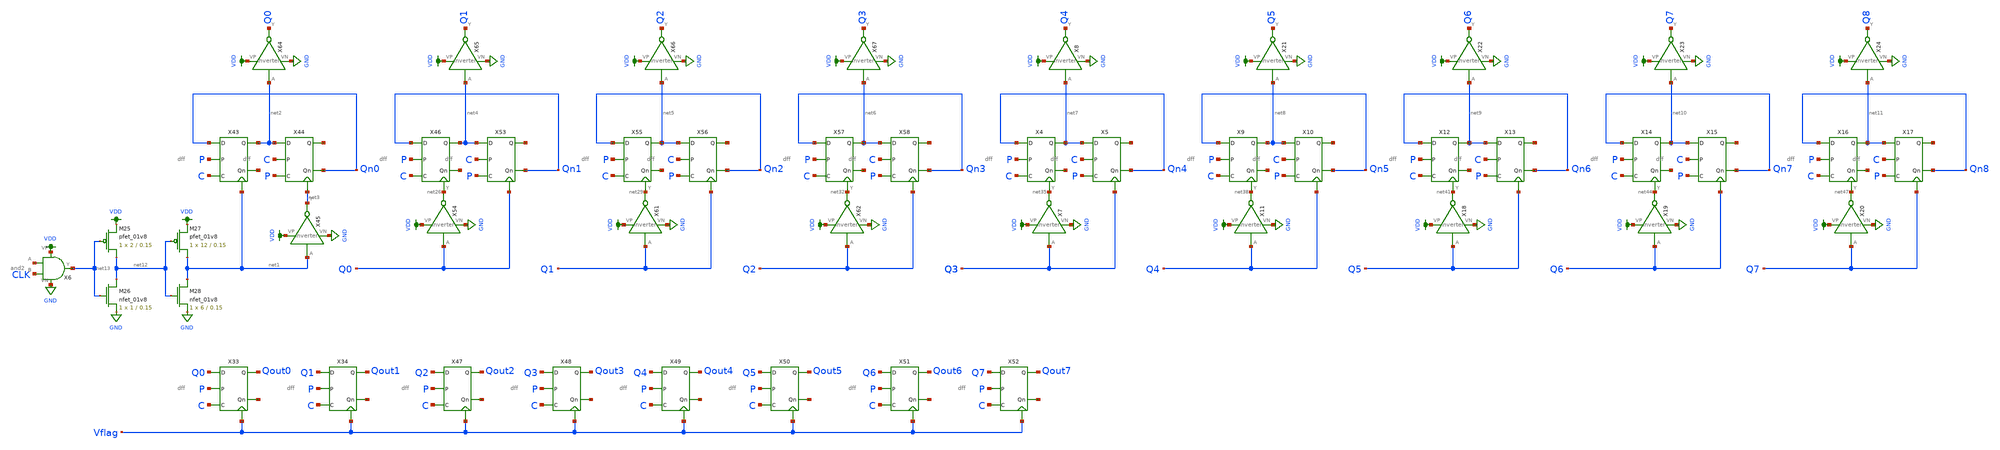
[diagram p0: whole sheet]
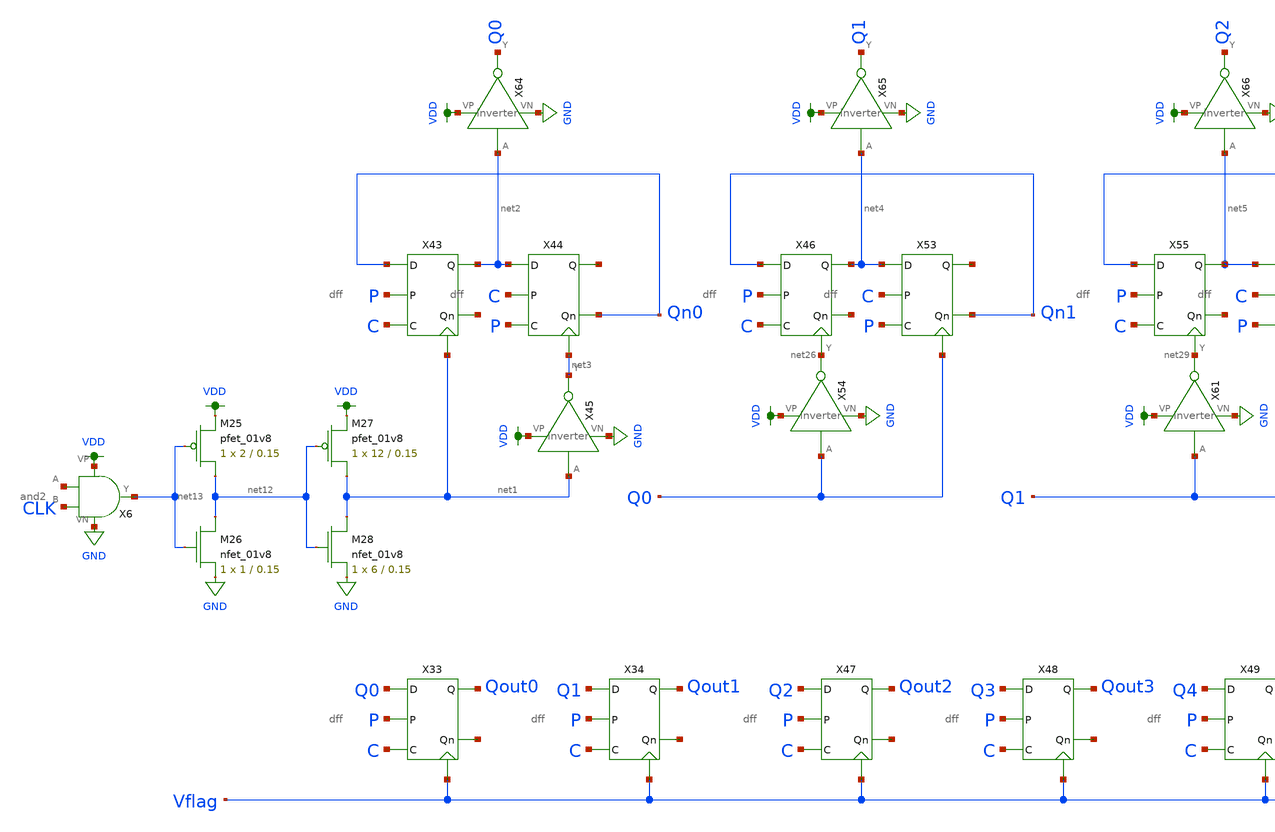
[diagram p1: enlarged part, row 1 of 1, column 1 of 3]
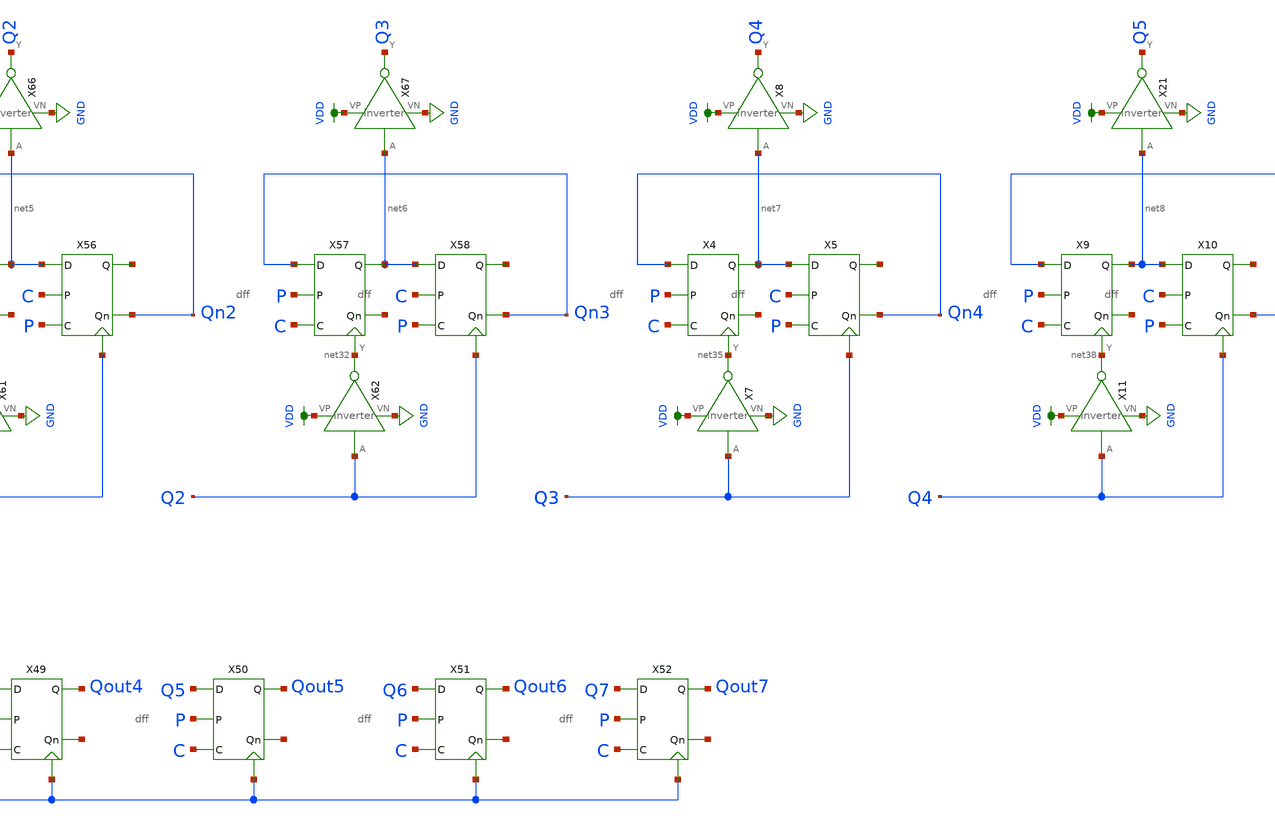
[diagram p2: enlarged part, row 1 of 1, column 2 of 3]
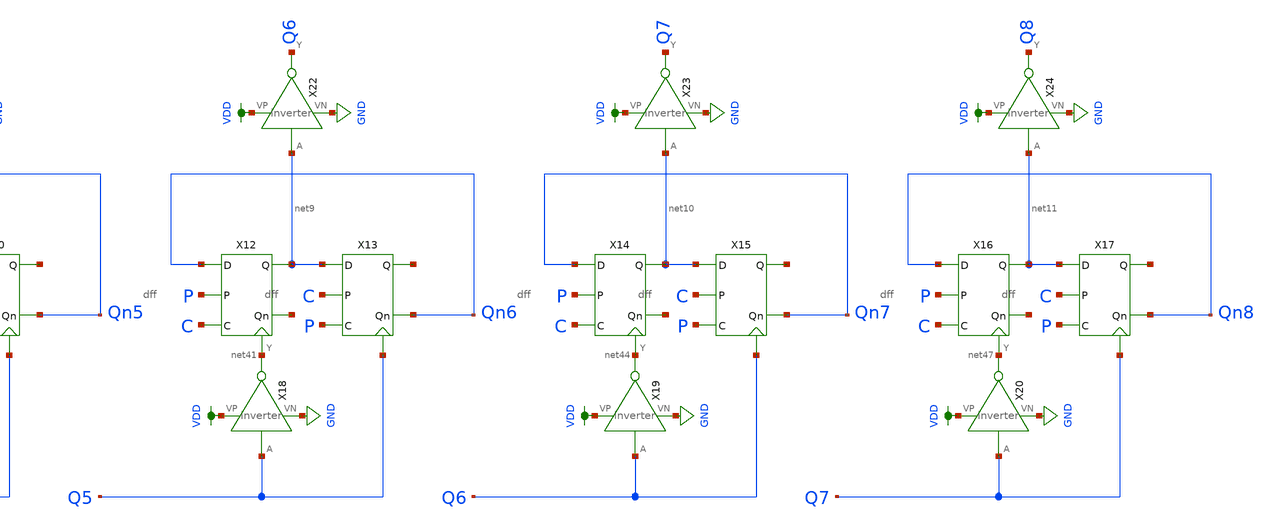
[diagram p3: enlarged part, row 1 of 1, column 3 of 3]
** sch_path: schematic/adc_digital_lvs.sch
**.subckt adc_digital_lvs
X6 VDD net14 GND net13 CLK and2
X33 Q0 net15 Qout0 Vflag P C dff
X34 Q1 net16 Qout1 Vflag P C dff
X47 Q2 net17 Qout2 Vflag P C dff
X48 Q3 net18 Qout3 Vflag P C dff
X49 Q4 net19 Qout4 Vflag P C dff
X50 Q5 net20 Qout5 Vflag P C dff
X51 Q6 net21 Qout6 Vflag P C dff
X52 Q7 net22 Qout7 Vflag P C dff
X43 Qn0 net23 net2 net1 P C dff
X44 net2 Qn0 net24 net3 C P dff
X45 net1 net3 VDD GND inverter
X46 Qn1 net25 net4 net26 P C dff
X53 net4 Qn1 net27 Q0 C P dff
X54 Q0 net26 VDD GND inverter
X55 Qn2 net28 net5 net29 P C dff
X56 net5 Qn2 net30 Q1 C P dff
X57 Qn3 net31 net6 net32 P C dff
X58 net6 Qn3 net33 Q2 C P dff
X61 Q1 net29 VDD GND inverter
X62 Q2 net32 VDD GND inverter
X64 net2 Q0 VDD GND inverter
X65 net4 Q1 VDD GND inverter
X66 net5 Q2 VDD GND inverter
X67 net6 Q3 VDD GND inverter
X4 Qn4 net34 net7 net35 P C dff
X5 net7 Qn4 net36 Q3 C P dff
X7 Q3 net35 VDD GND inverter
X8 net7 Q4 VDD GND inverter
X9 Qn5 net37 net8 net38 P C dff
X10 net8 Qn5 net39 Q4 C P dff
X11 Q4 net38 VDD GND inverter
X12 Qn6 net40 net9 net41 P C dff
X13 net9 Qn6 net42 Q5 C P dff
X14 Qn7 net43 net10 net44 P C dff
X15 net10 Qn7 net45 Q6 C P dff
X18 Q5 net41 VDD GND inverter
X19 Q6 net44 VDD GND inverter
X21 net8 Q5 VDD GND inverter
X22 net9 Q6 VDD GND inverter
X23 net10 Q7 VDD GND inverter
X16 Qn8 net46 net11 net47 P C dff
X17 net11 Qn8 net48 Q7 C P dff
X20 Q7 net47 VDD GND inverter
X24 net11 Q8 VDD GND inverter
XM25 net12 net13 VDD VDD sky130_fd_pr__pfet_01v8 L=0.15 W=2 nf=1 ad='int((nf+1)/2) * W/nf * 0.29' as='int((nf+2)/2) * W/nf * 0.29'
+ pd='2*int((nf+1)/2) * (W/nf + 0.29)' ps='2*int((nf+2)/2) * (W/nf + 0.29)' nrd='0.29 / W' nrs='0.29 / W'
+ sa=0 sb=0 sd=0 mult=1 m=1
XM26 net12 net13 GND GND sky130_fd_pr__nfet_01v8 L=0.15 W=1 nf=1 ad='int((nf+1)/2) * W/nf * 0.29' as='int((nf+2)/2) * W/nf * 0.29'
+ pd='2*int((nf+1)/2) * (W/nf + 0.29)' ps='2*int((nf+2)/2) * (W/nf + 0.29)' nrd='0.29 / W' nrs='0.29 / W'
+ sa=0 sb=0 sd=0 mult=1 m=1
XM27 net1 net12 VDD VDD sky130_fd_pr__pfet_01v8 L=0.15 W=12 nf=1 ad='int((nf+1)/2) * W/nf * 0.29' as='int((nf+2)/2) * W/nf * 0.29'
+ pd='2*int((nf+1)/2) * (W/nf + 0.29)' ps='2*int((nf+2)/2) * (W/nf + 0.29)' nrd='0.29 / W' nrs='0.29 / W'
+ sa=0 sb=0 sd=0 mult=1 m=1
XM28 net1 net12 GND GND sky130_fd_pr__nfet_01v8 L=0.15 W=6 nf=1 ad='int((nf+1)/2) * W/nf * 0.29' as='int((nf+2)/2) * W/nf * 0.29'
+ pd='2*int((nf+1)/2) * (W/nf + 0.29)' ps='2*int((nf+2)/2) * (W/nf + 0.29)' nrd='0.29 / W' nrs='0.29 / W'
+ sa=0 sb=0 sd=0 mult=1 m=1
**.ends
.GLOBAL VDD
.GLOBAL GND
.end
